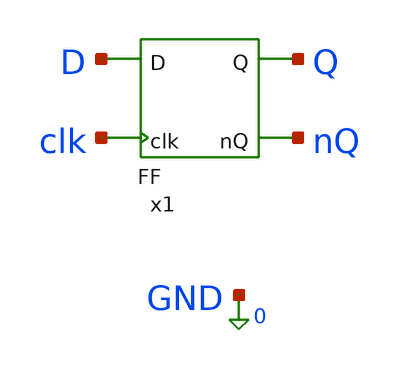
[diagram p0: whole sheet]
** sch_path: xschem_designs/FF_TB.sch
**.subckt FF_TB
x1 D Q nQ clk FF
**** begin user architecture code


.global VDD GND BP BN
.option temp=27
.include /usr/local/share/pdk/gf180mcuC/libs.tech/ngspice/design.ngspice
.lib /usr/local/share/pdk/gf180mcuC/libs.tech/ngspice/sm141064.ngspice typical

Vdd VDD 0 3.3
Vbp BP VDD 2.7
Vbn BN GND -2.7
VD D 0 PWL(0n 0 14.9n 0 15.1n 1.4 74.9n 1.4 75.1n 3.3 134.9n 3.3 135.1n 1.4 194.9n 1.4 195.1n 0
+ 254.9n 0 255.1n 3.3 314.9n 3.3 315.1n 0 374.9n 0 375.1n 0 434.9ns 0 435.1n 1.4 494.9n 1.4 495.1n 1.4
+ 554.9n 1.4 555.1n 3.3 615n 3.3)
Vclk clk 0 PULSE(3.3 0 29.9n 0.2n 0.2n 29.8n 60n)

.control
  save all
  tran 0.05n 615n
  write FF_TB.raw
.endc
.end


**** end user architecture code
**.ends

* expanding   symbol:  xschem_designs/FF.sym # of pins=4
** sym_path: xschem_designs/FF.sym
** sch_path: xschem_designs/FF.sch
.subckt FF D Q nQ clk
*.opin nQ
*.opin Q
*.ipin clk
*.ipin D
XM21 nclk clk VDD VDD pfet_03v3 L=0.28u W=0.44u nf=1 ad='int((nf+1)/2) * W/nf * 0.18u' as='int((nf+2)/2) * W/nf * 0.18u'
+ pd='2*int((nf+1)/2) * (W/nf + 0.18u)' ps='2*int((nf+2)/2) * (W/nf + 0.18u)' nrd='0.18u / W' nrs='0.18u / W'
+ sa=0 sb=0 sd=0 m=1 par=1
XM29 nclk clk GND GND nfet_03v3 L=0.28u W=0.22u nf=1 ad='int((nf+1)/2) * W/nf * 0.18u' as='int((nf+2)/2) * W/nf * 0.18u'
+ pd='2*int((nf+1)/2) * (W/nf + 0.18u)' ps='2*int((nf+2)/2) * (W/nf + 0.18u)' nrd='0.18u / W' nrs='0.18u / W'
+ sa=0 sb=0 sd=0 m=1 par=1
XM1 net1 nQ VDD VDD pfet_03v3 L=0.28u W=0.44u nf=1 ad='int((nf+1)/2) * W/nf * 0.18u' as='int((nf+2)/2) * W/nf * 0.18u'
+ pd='2*int((nf+1)/2) * (W/nf + 0.18u)' ps='2*int((nf+2)/2) * (W/nf + 0.18u)' nrd='0.18u / W' nrs='0.18u / W'
+ sa=0 sb=0 sd=0 m=1 par=1
XM22 Q Q net1 VDD pfet_03v3 L=2.24u W=0.44u nf=1 ad='int((nf+1)/2) * W/nf * 0.18u' as='int((nf+2)/2) * W/nf * 0.18u'
+ pd='2*int((nf+1)/2) * (W/nf + 0.18u)' ps='2*int((nf+2)/2) * (W/nf + 0.18u)' nrd='0.18u / W' nrs='0.18u / W'
+ sa=0 sb=0 sd=0 m=1 par=1
XM23 Q nQ VDD BP pfet_06v0 L=1.1u W=0.60u nf=1 ad='int((nf+1)/2) * W/nf * 0.18u' as='int((nf+2)/2) * W/nf * 0.18u'
+ pd='2*int((nf+1)/2) * (W/nf + 0.18u)' ps='2*int((nf+2)/2) * (W/nf + 0.18u)' nrd='0.18u / W' nrs='0.18u / W'
+ sa=0 sb=0 sd=0 m=1 par=1
XM24 Q S2 VDD BP pfet_06v0 L=1.1u W=0.60u nf=1 ad='int((nf+1)/2) * W/nf * 0.18u' as='int((nf+2)/2) * W/nf * 0.18u'
+ pd='2*int((nf+1)/2) * (W/nf + 0.18u)' ps='2*int((nf+2)/2) * (W/nf + 0.18u)' nrd='0.18u / W' nrs='0.18u / W'
+ sa=0 sb=0 sd=0 m=1 par=1
XM25 net1 S2 VDD VDD pfet_03v3 L=0.28u W=0.44u nf=1 ad='int((nf+1)/2) * W/nf * 0.18u' as='int((nf+2)/2) * W/nf * 0.18u'
+ pd='2*int((nf+1)/2) * (W/nf + 0.18u)' ps='2*int((nf+2)/2) * (W/nf + 0.18u)' nrd='0.18u / W' nrs='0.18u / W'
+ sa=0 sb=0 sd=0 m=1 par=1
XM26 Q Q net9 GND nfet_03v3 L=2.24u W=0.22u nf=1 ad='int((nf+1)/2) * W/nf * 0.18u' as='int((nf+2)/2) * W/nf * 0.18u'
+ pd='2*int((nf+1)/2) * (W/nf + 0.18u)' ps='2*int((nf+2)/2) * (W/nf + 0.18u)' nrd='0.18u / W' nrs='0.18u / W'
+ sa=0 sb=0 sd=0 m=1 par=1
XM27 net10 nQ GND BN nfet_06v0 L=1.4u W=0.30u nf=1 ad='int((nf+1)/2) * W/nf * 0.18u' as='int((nf+2)/2) * W/nf * 0.18u'
+ pd='2*int((nf+1)/2) * (W/nf + 0.18u)' ps='2*int((nf+2)/2) * (W/nf + 0.18u)' nrd='0.18u / W' nrs='0.18u / W'
+ sa=0 sb=0 sd=0 m=1 par=1
XM28 Q S2 net10 BN nfet_06v0 L=1.4u W=0.30u nf=1 ad='int((nf+1)/2) * W/nf * 0.18u' as='int((nf+2)/2) * W/nf * 0.18u'
+ pd='2*int((nf+1)/2) * (W/nf + 0.18u)' ps='2*int((nf+2)/2) * (W/nf + 0.18u)' nrd='0.18u / W' nrs='0.18u / W'
+ sa=0 sb=0 sd=0 m=1 par=1
XM2 net11 nQ GND GND nfet_03v3 L=0.28u W=0.22u nf=1 ad='int((nf+1)/2) * W/nf * 0.18u' as='int((nf+2)/2) * W/nf * 0.18u'
+ pd='2*int((nf+1)/2) * (W/nf + 0.18u)' ps='2*int((nf+2)/2) * (W/nf + 0.18u)' nrd='0.18u / W' nrs='0.18u / W'
+ sa=0 sb=0 sd=0 m=1 par=1
XM30 net9 S2 net11 GND nfet_03v3 L=0.28u W=0.22u nf=1 ad='int((nf+1)/2) * W/nf * 0.18u' as='int((nf+2)/2) * W/nf * 0.18u'
+ pd='2*int((nf+1)/2) * (W/nf + 0.18u)' ps='2*int((nf+2)/2) * (W/nf + 0.18u)' nrd='0.18u / W' nrs='0.18u / W'
+ sa=0 sb=0 sd=0 m=1 par=1
XM225 nD nD net12 GND nfet_03v3 L=2.24u W=0.22u nf=1 ad='int((nf+1)/2) * W/nf * 0.18u' as='int((nf+2)/2) * W/nf * 0.18u'
+ pd='2*int((nf+1)/2) * (W/nf + 0.18u)' ps='2*int((nf+2)/2) * (W/nf + 0.18u)' nrd='0.18u / W' nrs='0.18u / W'
+ sa=0 sb=0 sd=0 m=1 par=1
XM226 nD nD net13 VDD pfet_03v3 L=1.12u W=0.22u nf=1 ad='int((nf+1)/2) * W/nf * 0.18u' as='int((nf+2)/2) * W/nf * 0.18u'
+ pd='2*int((nf+1)/2) * (W/nf + 0.18u)' ps='2*int((nf+2)/2) * (W/nf + 0.18u)' nrd='0.18u / W' nrs='0.18u / W'
+ sa=0 sb=0 sd=0 m=1 par=1
XM237 net13 D VDD VDD pfet_03v3 L=0.28u W=0.44u nf=1 ad='int((nf+1)/2) * W/nf * 0.18u' as='int((nf+2)/2) * W/nf * 0.18u'
+ pd='2*int((nf+1)/2) * (W/nf + 0.18u)' ps='2*int((nf+2)/2) * (W/nf + 0.18u)' nrd='0.18u / W' nrs='0.18u / W'
+ sa=0 sb=0 sd=0 m=1 par=1
XM238 net12 D GND GND nfet_03v3 L=0.28u W=0.22u nf=1 ad='int((nf+1)/2) * W/nf * 0.18u' as='int((nf+2)/2) * W/nf * 0.18u'
+ pd='2*int((nf+1)/2) * (W/nf + 0.18u)' ps='2*int((nf+2)/2) * (W/nf + 0.18u)' nrd='0.18u / W' nrs='0.18u / W'
+ sa=0 sb=0 sd=0 m=1 par=1
XM241 nD D VDD BP pfet_06v0 L=1.1u W=0.60u nf=1 ad='int((nf+1)/2) * W/nf * 0.18u' as='int((nf+2)/2) * W/nf * 0.18u'
+ pd='2*int((nf+1)/2) * (W/nf + 0.18u)' ps='2*int((nf+2)/2) * (W/nf + 0.18u)' nrd='0.18u / W' nrs='0.18u / W'
+ sa=0 sb=0 sd=0 m=1 par=1
XM242 nD D GND BN nfet_06v0 L=1.4u W=0.30u nf=1 ad='int((nf+1)/2) * W/nf * 0.18u' as='int((nf+2)/2) * W/nf * 0.18u'
+ pd='2*int((nf+1)/2) * (W/nf + 0.18u)' ps='2*int((nf+2)/2) * (W/nf + 0.18u)' nrd='0.18u / W' nrs='0.18u / W'
+ sa=0 sb=0 sd=0 m=1 par=1
XM3 net2 Q VDD VDD pfet_03v3 L=0.28u W=0.44u nf=1 ad='int((nf+1)/2) * W/nf * 0.18u' as='int((nf+2)/2) * W/nf * 0.18u'
+ pd='2*int((nf+1)/2) * (W/nf + 0.18u)' ps='2*int((nf+2)/2) * (W/nf + 0.18u)' nrd='0.18u / W' nrs='0.18u / W'
+ sa=0 sb=0 sd=0 m=1 par=1
XM4 nQ nQ net2 VDD pfet_03v3 L=2.24u W=0.44u nf=1 ad='int((nf+1)/2) * W/nf * 0.18u' as='int((nf+2)/2) * W/nf * 0.18u'
+ pd='2*int((nf+1)/2) * (W/nf + 0.18u)' ps='2*int((nf+2)/2) * (W/nf + 0.18u)' nrd='0.18u / W' nrs='0.18u / W'
+ sa=0 sb=0 sd=0 m=1 par=1
XM5 nQ Q VDD BP pfet_06v0 L=1.1u W=0.60u nf=1 ad='int((nf+1)/2) * W/nf * 0.18u' as='int((nf+2)/2) * W/nf * 0.18u'
+ pd='2*int((nf+1)/2) * (W/nf + 0.18u)' ps='2*int((nf+2)/2) * (W/nf + 0.18u)' nrd='0.18u / W' nrs='0.18u / W'
+ sa=0 sb=0 sd=0 m=1 par=1
XM6 nQ R2 VDD BP pfet_06v0 L=1.1u W=0.60u nf=1 ad='int((nf+1)/2) * W/nf * 0.18u' as='int((nf+2)/2) * W/nf * 0.18u'
+ pd='2*int((nf+1)/2) * (W/nf + 0.18u)' ps='2*int((nf+2)/2) * (W/nf + 0.18u)' nrd='0.18u / W' nrs='0.18u / W'
+ sa=0 sb=0 sd=0 m=1 par=1
XM7 net2 R2 VDD VDD pfet_03v3 L=0.28u W=0.44u nf=1 ad='int((nf+1)/2) * W/nf * 0.18u' as='int((nf+2)/2) * W/nf * 0.18u'
+ pd='2*int((nf+1)/2) * (W/nf + 0.18u)' ps='2*int((nf+2)/2) * (W/nf + 0.18u)' nrd='0.18u / W' nrs='0.18u / W'
+ sa=0 sb=0 sd=0 m=1 par=1
XM8 nQ nQ net14 GND nfet_03v3 L=2.24u W=0.22u nf=1 ad='int((nf+1)/2) * W/nf * 0.18u' as='int((nf+2)/2) * W/nf * 0.18u'
+ pd='2*int((nf+1)/2) * (W/nf + 0.18u)' ps='2*int((nf+2)/2) * (W/nf + 0.18u)' nrd='0.18u / W' nrs='0.18u / W'
+ sa=0 sb=0 sd=0 m=1 par=1
XM9 net15 Q GND BN nfet_06v0 L=1.4u W=0.30u nf=1 ad='int((nf+1)/2) * W/nf * 0.18u' as='int((nf+2)/2) * W/nf * 0.18u'
+ pd='2*int((nf+1)/2) * (W/nf + 0.18u)' ps='2*int((nf+2)/2) * (W/nf + 0.18u)' nrd='0.18u / W' nrs='0.18u / W'
+ sa=0 sb=0 sd=0 m=1 par=1
XM10 nQ R2 net15 BN nfet_06v0 L=1.4u W=0.30u nf=1 ad='int((nf+1)/2) * W/nf * 0.18u' as='int((nf+2)/2) * W/nf * 0.18u'
+ pd='2*int((nf+1)/2) * (W/nf + 0.18u)' ps='2*int((nf+2)/2) * (W/nf + 0.18u)' nrd='0.18u / W' nrs='0.18u / W'
+ sa=0 sb=0 sd=0 m=1 par=1
XM11 net16 Q GND GND nfet_03v3 L=0.28u W=0.22u nf=1 ad='int((nf+1)/2) * W/nf * 0.18u' as='int((nf+2)/2) * W/nf * 0.18u'
+ pd='2*int((nf+1)/2) * (W/nf + 0.18u)' ps='2*int((nf+2)/2) * (W/nf + 0.18u)' nrd='0.18u / W' nrs='0.18u / W'
+ sa=0 sb=0 sd=0 m=1 par=1
XM12 net14 R2 net16 GND nfet_03v3 L=0.28u W=0.22u nf=1 ad='int((nf+1)/2) * W/nf * 0.18u' as='int((nf+2)/2) * W/nf * 0.18u'
+ pd='2*int((nf+1)/2) * (W/nf + 0.18u)' ps='2*int((nf+2)/2) * (W/nf + 0.18u)' nrd='0.18u / W' nrs='0.18u / W'
+ sa=0 sb=0 sd=0 m=1 par=1
XM13 net3 Qi VDD VDD pfet_03v3 L=0.28u W=0.44u nf=1 ad='int((nf+1)/2) * W/nf * 0.18u' as='int((nf+2)/2) * W/nf * 0.18u'
+ pd='2*int((nf+1)/2) * (W/nf + 0.18u)' ps='2*int((nf+2)/2) * (W/nf + 0.18u)' nrd='0.18u / W' nrs='0.18u / W'
+ sa=0 sb=0 sd=0 m=1 par=1
XM14 S2 S2 net3 VDD pfet_03v3 L=2.24u W=0.44u nf=1 ad='int((nf+1)/2) * W/nf * 0.18u' as='int((nf+2)/2) * W/nf * 0.18u'
+ pd='2*int((nf+1)/2) * (W/nf + 0.18u)' ps='2*int((nf+2)/2) * (W/nf + 0.18u)' nrd='0.18u / W' nrs='0.18u / W'
+ sa=0 sb=0 sd=0 m=1 par=1
XM15 S2 Qi VDD BP pfet_06v0 L=1.1u W=0.60u nf=1 ad='int((nf+1)/2) * W/nf * 0.18u' as='int((nf+2)/2) * W/nf * 0.18u'
+ pd='2*int((nf+1)/2) * (W/nf + 0.18u)' ps='2*int((nf+2)/2) * (W/nf + 0.18u)' nrd='0.18u / W' nrs='0.18u / W'
+ sa=0 sb=0 sd=0 m=1 par=1
XM16 S2 nclk VDD BP pfet_06v0 L=1.1u W=0.60u nf=1 ad='int((nf+1)/2) * W/nf * 0.18u' as='int((nf+2)/2) * W/nf * 0.18u'
+ pd='2*int((nf+1)/2) * (W/nf + 0.18u)' ps='2*int((nf+2)/2) * (W/nf + 0.18u)' nrd='0.18u / W' nrs='0.18u / W'
+ sa=0 sb=0 sd=0 m=1 par=1
XM17 net3 nclk VDD VDD pfet_03v3 L=0.28u W=0.44u nf=1 ad='int((nf+1)/2) * W/nf * 0.18u' as='int((nf+2)/2) * W/nf * 0.18u'
+ pd='2*int((nf+1)/2) * (W/nf + 0.18u)' ps='2*int((nf+2)/2) * (W/nf + 0.18u)' nrd='0.18u / W' nrs='0.18u / W'
+ sa=0 sb=0 sd=0 m=1 par=1
XM18 S2 S2 net17 GND nfet_03v3 L=2.24u W=0.22u nf=1 ad='int((nf+1)/2) * W/nf * 0.18u' as='int((nf+2)/2) * W/nf * 0.18u'
+ pd='2*int((nf+1)/2) * (W/nf + 0.18u)' ps='2*int((nf+2)/2) * (W/nf + 0.18u)' nrd='0.18u / W' nrs='0.18u / W'
+ sa=0 sb=0 sd=0 m=1 par=1
XM19 net18 Qi GND BN nfet_06v0 L=1.4u W=0.30u nf=1 ad='int((nf+1)/2) * W/nf * 0.18u' as='int((nf+2)/2) * W/nf * 0.18u'
+ pd='2*int((nf+1)/2) * (W/nf + 0.18u)' ps='2*int((nf+2)/2) * (W/nf + 0.18u)' nrd='0.18u / W' nrs='0.18u / W'
+ sa=0 sb=0 sd=0 m=1 par=1
XM20 S2 nclk net18 BN nfet_06v0 L=1.4u W=0.30u nf=1 ad='int((nf+1)/2) * W/nf * 0.18u' as='int((nf+2)/2) * W/nf * 0.18u'
+ pd='2*int((nf+1)/2) * (W/nf + 0.18u)' ps='2*int((nf+2)/2) * (W/nf + 0.18u)' nrd='0.18u / W' nrs='0.18u / W'
+ sa=0 sb=0 sd=0 m=1 par=1
XM31 net19 Qi GND GND nfet_03v3 L=0.28u W=0.22u nf=1 ad='int((nf+1)/2) * W/nf * 0.18u' as='int((nf+2)/2) * W/nf * 0.18u'
+ pd='2*int((nf+1)/2) * (W/nf + 0.18u)' ps='2*int((nf+2)/2) * (W/nf + 0.18u)' nrd='0.18u / W' nrs='0.18u / W'
+ sa=0 sb=0 sd=0 m=1 par=1
XM32 net17 nclk net19 GND nfet_03v3 L=0.28u W=0.22u nf=1 ad='int((nf+1)/2) * W/nf * 0.18u' as='int((nf+2)/2) * W/nf * 0.18u'
+ pd='2*int((nf+1)/2) * (W/nf + 0.18u)' ps='2*int((nf+2)/2) * (W/nf + 0.18u)' nrd='0.18u / W' nrs='0.18u / W'
+ sa=0 sb=0 sd=0 m=1 par=1
XM33 net4 nQi VDD VDD pfet_03v3 L=0.28u W=0.44u nf=1 ad='int((nf+1)/2) * W/nf * 0.18u' as='int((nf+2)/2) * W/nf * 0.18u'
+ pd='2*int((nf+1)/2) * (W/nf + 0.18u)' ps='2*int((nf+2)/2) * (W/nf + 0.18u)' nrd='0.18u / W' nrs='0.18u / W'
+ sa=0 sb=0 sd=0 m=1 par=1
XM34 R2 R2 net4 VDD pfet_03v3 L=2.24u W=0.44u nf=1 ad='int((nf+1)/2) * W/nf * 0.18u' as='int((nf+2)/2) * W/nf * 0.18u'
+ pd='2*int((nf+1)/2) * (W/nf + 0.18u)' ps='2*int((nf+2)/2) * (W/nf + 0.18u)' nrd='0.18u / W' nrs='0.18u / W'
+ sa=0 sb=0 sd=0 m=1 par=1
XM35 R2 nQi VDD BP pfet_06v0 L=1.1u W=0.60u nf=1 ad='int((nf+1)/2) * W/nf * 0.18u' as='int((nf+2)/2) * W/nf * 0.18u'
+ pd='2*int((nf+1)/2) * (W/nf + 0.18u)' ps='2*int((nf+2)/2) * (W/nf + 0.18u)' nrd='0.18u / W' nrs='0.18u / W'
+ sa=0 sb=0 sd=0 m=1 par=1
XM36 R2 nclk VDD BP pfet_06v0 L=1.1u W=0.60u nf=1 ad='int((nf+1)/2) * W/nf * 0.18u' as='int((nf+2)/2) * W/nf * 0.18u'
+ pd='2*int((nf+1)/2) * (W/nf + 0.18u)' ps='2*int((nf+2)/2) * (W/nf + 0.18u)' nrd='0.18u / W' nrs='0.18u / W'
+ sa=0 sb=0 sd=0 m=1 par=1
XM37 net4 nclk VDD VDD pfet_03v3 L=0.28u W=0.44u nf=1 ad='int((nf+1)/2) * W/nf * 0.18u' as='int((nf+2)/2) * W/nf * 0.18u'
+ pd='2*int((nf+1)/2) * (W/nf + 0.18u)' ps='2*int((nf+2)/2) * (W/nf + 0.18u)' nrd='0.18u / W' nrs='0.18u / W'
+ sa=0 sb=0 sd=0 m=1 par=1
XM38 R2 R2 net20 GND nfet_03v3 L=2.24u W=0.22u nf=1 ad='int((nf+1)/2) * W/nf * 0.18u' as='int((nf+2)/2) * W/nf * 0.18u'
+ pd='2*int((nf+1)/2) * (W/nf + 0.18u)' ps='2*int((nf+2)/2) * (W/nf + 0.18u)' nrd='0.18u / W' nrs='0.18u / W'
+ sa=0 sb=0 sd=0 m=1 par=1
XM39 net21 nQi GND BN nfet_06v0 L=1.4u W=0.30u nf=1 ad='int((nf+1)/2) * W/nf * 0.18u' as='int((nf+2)/2) * W/nf * 0.18u'
+ pd='2*int((nf+1)/2) * (W/nf + 0.18u)' ps='2*int((nf+2)/2) * (W/nf + 0.18u)' nrd='0.18u / W' nrs='0.18u / W'
+ sa=0 sb=0 sd=0 m=1 par=1
XM40 R2 nclk net21 BN nfet_06v0 L=1.4u W=0.30u nf=1 ad='int((nf+1)/2) * W/nf * 0.18u' as='int((nf+2)/2) * W/nf * 0.18u'
+ pd='2*int((nf+1)/2) * (W/nf + 0.18u)' ps='2*int((nf+2)/2) * (W/nf + 0.18u)' nrd='0.18u / W' nrs='0.18u / W'
+ sa=0 sb=0 sd=0 m=1 par=1
XM41 net22 nQi GND GND nfet_03v3 L=0.28u W=0.22u nf=1 ad='int((nf+1)/2) * W/nf * 0.18u' as='int((nf+2)/2) * W/nf * 0.18u'
+ pd='2*int((nf+1)/2) * (W/nf + 0.18u)' ps='2*int((nf+2)/2) * (W/nf + 0.18u)' nrd='0.18u / W' nrs='0.18u / W'
+ sa=0 sb=0 sd=0 m=1 par=1
XM42 net20 nclk net22 GND nfet_03v3 L=0.28u W=0.22u nf=1 ad='int((nf+1)/2) * W/nf * 0.18u' as='int((nf+2)/2) * W/nf * 0.18u'
+ pd='2*int((nf+1)/2) * (W/nf + 0.18u)' ps='2*int((nf+2)/2) * (W/nf + 0.18u)' nrd='0.18u / W' nrs='0.18u / W'
+ sa=0 sb=0 sd=0 m=1 par=1
XM53 net5 nQi VDD VDD pfet_03v3 L=0.28u W=0.44u nf=1 ad='int((nf+1)/2) * W/nf * 0.18u' as='int((nf+2)/2) * W/nf * 0.18u'
+ pd='2*int((nf+1)/2) * (W/nf + 0.18u)' ps='2*int((nf+2)/2) * (W/nf + 0.18u)' nrd='0.18u / W' nrs='0.18u / W'
+ sa=0 sb=0 sd=0 m=1 par=1
XM54 Qi Qi net5 VDD pfet_03v3 L=2.24u W=0.44u nf=1 ad='int((nf+1)/2) * W/nf * 0.18u' as='int((nf+2)/2) * W/nf * 0.18u'
+ pd='2*int((nf+1)/2) * (W/nf + 0.18u)' ps='2*int((nf+2)/2) * (W/nf + 0.18u)' nrd='0.18u / W' nrs='0.18u / W'
+ sa=0 sb=0 sd=0 m=1 par=1
XM55 Qi nQi VDD BP pfet_06v0 L=1.1u W=0.60u nf=1 ad='int((nf+1)/2) * W/nf * 0.18u' as='int((nf+2)/2) * W/nf * 0.18u'
+ pd='2*int((nf+1)/2) * (W/nf + 0.18u)' ps='2*int((nf+2)/2) * (W/nf + 0.18u)' nrd='0.18u / W' nrs='0.18u / W'
+ sa=0 sb=0 sd=0 m=1 par=1
XM56 Qi S1 VDD BP pfet_06v0 L=1.1u W=0.60u nf=1 ad='int((nf+1)/2) * W/nf * 0.18u' as='int((nf+2)/2) * W/nf * 0.18u'
+ pd='2*int((nf+1)/2) * (W/nf + 0.18u)' ps='2*int((nf+2)/2) * (W/nf + 0.18u)' nrd='0.18u / W' nrs='0.18u / W'
+ sa=0 sb=0 sd=0 m=1 par=1
XM57 net5 S1 VDD VDD pfet_03v3 L=0.28u W=0.44u nf=1 ad='int((nf+1)/2) * W/nf * 0.18u' as='int((nf+2)/2) * W/nf * 0.18u'
+ pd='2*int((nf+1)/2) * (W/nf + 0.18u)' ps='2*int((nf+2)/2) * (W/nf + 0.18u)' nrd='0.18u / W' nrs='0.18u / W'
+ sa=0 sb=0 sd=0 m=1 par=1
XM58 Qi Qi net23 GND nfet_03v3 L=2.24u W=0.22u nf=1 ad='int((nf+1)/2) * W/nf * 0.18u' as='int((nf+2)/2) * W/nf * 0.18u'
+ pd='2*int((nf+1)/2) * (W/nf + 0.18u)' ps='2*int((nf+2)/2) * (W/nf + 0.18u)' nrd='0.18u / W' nrs='0.18u / W'
+ sa=0 sb=0 sd=0 m=1 par=1
XM59 net24 nQi GND BN nfet_06v0 L=1.4u W=0.30u nf=1 ad='int((nf+1)/2) * W/nf * 0.18u' as='int((nf+2)/2) * W/nf * 0.18u'
+ pd='2*int((nf+1)/2) * (W/nf + 0.18u)' ps='2*int((nf+2)/2) * (W/nf + 0.18u)' nrd='0.18u / W' nrs='0.18u / W'
+ sa=0 sb=0 sd=0 m=1 par=1
XM60 Qi S1 net24 BN nfet_06v0 L=1.4u W=0.30u nf=1 ad='int((nf+1)/2) * W/nf * 0.18u' as='int((nf+2)/2) * W/nf * 0.18u'
+ pd='2*int((nf+1)/2) * (W/nf + 0.18u)' ps='2*int((nf+2)/2) * (W/nf + 0.18u)' nrd='0.18u / W' nrs='0.18u / W'
+ sa=0 sb=0 sd=0 m=1 par=1
XM61 net25 nQi GND GND nfet_03v3 L=0.28u W=0.22u nf=1 ad='int((nf+1)/2) * W/nf * 0.18u' as='int((nf+2)/2) * W/nf * 0.18u'
+ pd='2*int((nf+1)/2) * (W/nf + 0.18u)' ps='2*int((nf+2)/2) * (W/nf + 0.18u)' nrd='0.18u / W' nrs='0.18u / W'
+ sa=0 sb=0 sd=0 m=1 par=1
XM62 net23 S1 net25 GND nfet_03v3 L=0.28u W=0.22u nf=1 ad='int((nf+1)/2) * W/nf * 0.18u' as='int((nf+2)/2) * W/nf * 0.18u'
+ pd='2*int((nf+1)/2) * (W/nf + 0.18u)' ps='2*int((nf+2)/2) * (W/nf + 0.18u)' nrd='0.18u / W' nrs='0.18u / W'
+ sa=0 sb=0 sd=0 m=1 par=1
XM63 net6 Qi VDD VDD pfet_03v3 L=0.28u W=0.44u nf=1 ad='int((nf+1)/2) * W/nf * 0.18u' as='int((nf+2)/2) * W/nf * 0.18u'
+ pd='2*int((nf+1)/2) * (W/nf + 0.18u)' ps='2*int((nf+2)/2) * (W/nf + 0.18u)' nrd='0.18u / W' nrs='0.18u / W'
+ sa=0 sb=0 sd=0 m=1 par=1
XM64 nQi nQi net6 VDD pfet_03v3 L=2.24u W=0.44u nf=1 ad='int((nf+1)/2) * W/nf * 0.18u' as='int((nf+2)/2) * W/nf * 0.18u'
+ pd='2*int((nf+1)/2) * (W/nf + 0.18u)' ps='2*int((nf+2)/2) * (W/nf + 0.18u)' nrd='0.18u / W' nrs='0.18u / W'
+ sa=0 sb=0 sd=0 m=1 par=1
XM65 nQi Qi VDD BP pfet_06v0 L=1.1u W=0.60u nf=1 ad='int((nf+1)/2) * W/nf * 0.18u' as='int((nf+2)/2) * W/nf * 0.18u'
+ pd='2*int((nf+1)/2) * (W/nf + 0.18u)' ps='2*int((nf+2)/2) * (W/nf + 0.18u)' nrd='0.18u / W' nrs='0.18u / W'
+ sa=0 sb=0 sd=0 m=1 par=1
XM66 nQi R1 VDD BP pfet_06v0 L=1.1u W=0.60u nf=1 ad='int((nf+1)/2) * W/nf * 0.18u' as='int((nf+2)/2) * W/nf * 0.18u'
+ pd='2*int((nf+1)/2) * (W/nf + 0.18u)' ps='2*int((nf+2)/2) * (W/nf + 0.18u)' nrd='0.18u / W' nrs='0.18u / W'
+ sa=0 sb=0 sd=0 m=1 par=1
XM67 net6 R1 VDD VDD pfet_03v3 L=0.28u W=0.44u nf=1 ad='int((nf+1)/2) * W/nf * 0.18u' as='int((nf+2)/2) * W/nf * 0.18u'
+ pd='2*int((nf+1)/2) * (W/nf + 0.18u)' ps='2*int((nf+2)/2) * (W/nf + 0.18u)' nrd='0.18u / W' nrs='0.18u / W'
+ sa=0 sb=0 sd=0 m=1 par=1
XM68 nQi nQi net26 GND nfet_03v3 L=2.24u W=0.22u nf=1 ad='int((nf+1)/2) * W/nf * 0.18u' as='int((nf+2)/2) * W/nf * 0.18u'
+ pd='2*int((nf+1)/2) * (W/nf + 0.18u)' ps='2*int((nf+2)/2) * (W/nf + 0.18u)' nrd='0.18u / W' nrs='0.18u / W'
+ sa=0 sb=0 sd=0 m=1 par=1
XM69 net27 Qi GND BN nfet_06v0 L=1.4u W=0.30u nf=1 ad='int((nf+1)/2) * W/nf * 0.18u' as='int((nf+2)/2) * W/nf * 0.18u'
+ pd='2*int((nf+1)/2) * (W/nf + 0.18u)' ps='2*int((nf+2)/2) * (W/nf + 0.18u)' nrd='0.18u / W' nrs='0.18u / W'
+ sa=0 sb=0 sd=0 m=1 par=1
XM70 nQi R1 net27 BN nfet_06v0 L=1.4u W=0.30u nf=1 ad='int((nf+1)/2) * W/nf * 0.18u' as='int((nf+2)/2) * W/nf * 0.18u'
+ pd='2*int((nf+1)/2) * (W/nf + 0.18u)' ps='2*int((nf+2)/2) * (W/nf + 0.18u)' nrd='0.18u / W' nrs='0.18u / W'
+ sa=0 sb=0 sd=0 m=1 par=1
XM71 net28 Qi GND GND nfet_03v3 L=0.28u W=0.22u nf=1 ad='int((nf+1)/2) * W/nf * 0.18u' as='int((nf+2)/2) * W/nf * 0.18u'
+ pd='2*int((nf+1)/2) * (W/nf + 0.18u)' ps='2*int((nf+2)/2) * (W/nf + 0.18u)' nrd='0.18u / W' nrs='0.18u / W'
+ sa=0 sb=0 sd=0 m=1 par=1
XM72 net26 R1 net28 GND nfet_03v3 L=0.28u W=0.22u nf=1 ad='int((nf+1)/2) * W/nf * 0.18u' as='int((nf+2)/2) * W/nf * 0.18u'
+ pd='2*int((nf+1)/2) * (W/nf + 0.18u)' ps='2*int((nf+2)/2) * (W/nf + 0.18u)' nrd='0.18u / W' nrs='0.18u / W'
+ sa=0 sb=0 sd=0 m=1 par=1
XM73 net7 D VDD VDD pfet_03v3 L=0.28u W=0.44u nf=1 ad='int((nf+1)/2) * W/nf * 0.18u' as='int((nf+2)/2) * W/nf * 0.18u'
+ pd='2*int((nf+1)/2) * (W/nf + 0.18u)' ps='2*int((nf+2)/2) * (W/nf + 0.18u)' nrd='0.18u / W' nrs='0.18u / W'
+ sa=0 sb=0 sd=0 m=1 par=1
XM74 S1 S1 net7 VDD pfet_03v3 L=2.24u W=0.44u nf=1 ad='int((nf+1)/2) * W/nf * 0.18u' as='int((nf+2)/2) * W/nf * 0.18u'
+ pd='2*int((nf+1)/2) * (W/nf + 0.18u)' ps='2*int((nf+2)/2) * (W/nf + 0.18u)' nrd='0.18u / W' nrs='0.18u / W'
+ sa=0 sb=0 sd=0 m=1 par=1
XM75 S1 D VDD BP pfet_06v0 L=1.1u W=0.60u nf=1 ad='int((nf+1)/2) * W/nf * 0.18u' as='int((nf+2)/2) * W/nf * 0.18u'
+ pd='2*int((nf+1)/2) * (W/nf + 0.18u)' ps='2*int((nf+2)/2) * (W/nf + 0.18u)' nrd='0.18u / W' nrs='0.18u / W'
+ sa=0 sb=0 sd=0 m=1 par=1
XM76 S1 clk VDD BP pfet_06v0 L=1.1u W=0.60u nf=1 ad='int((nf+1)/2) * W/nf * 0.18u' as='int((nf+2)/2) * W/nf * 0.18u'
+ pd='2*int((nf+1)/2) * (W/nf + 0.18u)' ps='2*int((nf+2)/2) * (W/nf + 0.18u)' nrd='0.18u / W' nrs='0.18u / W'
+ sa=0 sb=0 sd=0 m=1 par=1
XM77 net7 clk VDD VDD pfet_03v3 L=0.28u W=0.44u nf=1 ad='int((nf+1)/2) * W/nf * 0.18u' as='int((nf+2)/2) * W/nf * 0.18u'
+ pd='2*int((nf+1)/2) * (W/nf + 0.18u)' ps='2*int((nf+2)/2) * (W/nf + 0.18u)' nrd='0.18u / W' nrs='0.18u / W'
+ sa=0 sb=0 sd=0 m=1 par=1
XM78 S1 S1 net29 GND nfet_03v3 L=2.24u W=0.22u nf=1 ad='int((nf+1)/2) * W/nf * 0.18u' as='int((nf+2)/2) * W/nf * 0.18u'
+ pd='2*int((nf+1)/2) * (W/nf + 0.18u)' ps='2*int((nf+2)/2) * (W/nf + 0.18u)' nrd='0.18u / W' nrs='0.18u / W'
+ sa=0 sb=0 sd=0 m=1 par=1
XM79 net30 D GND BN nfet_06v0 L=1.4u W=0.30u nf=1 ad='int((nf+1)/2) * W/nf * 0.18u' as='int((nf+2)/2) * W/nf * 0.18u'
+ pd='2*int((nf+1)/2) * (W/nf + 0.18u)' ps='2*int((nf+2)/2) * (W/nf + 0.18u)' nrd='0.18u / W' nrs='0.18u / W'
+ sa=0 sb=0 sd=0 m=1 par=1
XM80 S1 clk net30 BN nfet_06v0 L=1.4u W=0.30u nf=1 ad='int((nf+1)/2) * W/nf * 0.18u' as='int((nf+2)/2) * W/nf * 0.18u'
+ pd='2*int((nf+1)/2) * (W/nf + 0.18u)' ps='2*int((nf+2)/2) * (W/nf + 0.18u)' nrd='0.18u / W' nrs='0.18u / W'
+ sa=0 sb=0 sd=0 m=1 par=1
XM81 net31 D GND GND nfet_03v3 L=0.28u W=0.22u nf=1 ad='int((nf+1)/2) * W/nf * 0.18u' as='int((nf+2)/2) * W/nf * 0.18u'
+ pd='2*int((nf+1)/2) * (W/nf + 0.18u)' ps='2*int((nf+2)/2) * (W/nf + 0.18u)' nrd='0.18u / W' nrs='0.18u / W'
+ sa=0 sb=0 sd=0 m=1 par=1
XM82 net29 clk net31 GND nfet_03v3 L=0.28u W=0.22u nf=1 ad='int((nf+1)/2) * W/nf * 0.18u' as='int((nf+2)/2) * W/nf * 0.18u'
+ pd='2*int((nf+1)/2) * (W/nf + 0.18u)' ps='2*int((nf+2)/2) * (W/nf + 0.18u)' nrd='0.18u / W' nrs='0.18u / W'
+ sa=0 sb=0 sd=0 m=1 par=1
XM83 net8 nD VDD VDD pfet_03v3 L=0.28u W=0.44u nf=1 ad='int((nf+1)/2) * W/nf * 0.18u' as='int((nf+2)/2) * W/nf * 0.18u'
+ pd='2*int((nf+1)/2) * (W/nf + 0.18u)' ps='2*int((nf+2)/2) * (W/nf + 0.18u)' nrd='0.18u / W' nrs='0.18u / W'
+ sa=0 sb=0 sd=0 m=1 par=1
XM84 R1 R1 net8 VDD pfet_03v3 L=2.24u W=0.44u nf=1 ad='int((nf+1)/2) * W/nf * 0.18u' as='int((nf+2)/2) * W/nf * 0.18u'
+ pd='2*int((nf+1)/2) * (W/nf + 0.18u)' ps='2*int((nf+2)/2) * (W/nf + 0.18u)' nrd='0.18u / W' nrs='0.18u / W'
+ sa=0 sb=0 sd=0 m=1 par=1
XM85 R1 nD VDD BP pfet_06v0 L=1.1u W=0.60u nf=1 ad='int((nf+1)/2) * W/nf * 0.18u' as='int((nf+2)/2) * W/nf * 0.18u'
+ pd='2*int((nf+1)/2) * (W/nf + 0.18u)' ps='2*int((nf+2)/2) * (W/nf + 0.18u)' nrd='0.18u / W' nrs='0.18u / W'
+ sa=0 sb=0 sd=0 m=1 par=1
XM86 R1 clk VDD BP pfet_06v0 L=1.1u W=0.60u nf=1 ad='int((nf+1)/2) * W/nf * 0.18u' as='int((nf+2)/2) * W/nf * 0.18u'
+ pd='2*int((nf+1)/2) * (W/nf + 0.18u)' ps='2*int((nf+2)/2) * (W/nf + 0.18u)' nrd='0.18u / W' nrs='0.18u / W'
+ sa=0 sb=0 sd=0 m=1 par=1
XM87 net8 clk VDD VDD pfet_03v3 L=0.28u W=0.44u nf=1 ad='int((nf+1)/2) * W/nf * 0.18u' as='int((nf+2)/2) * W/nf * 0.18u'
+ pd='2*int((nf+1)/2) * (W/nf + 0.18u)' ps='2*int((nf+2)/2) * (W/nf + 0.18u)' nrd='0.18u / W' nrs='0.18u / W'
+ sa=0 sb=0 sd=0 m=1 par=1
XM88 R1 R1 net32 GND nfet_03v3 L=2.24u W=0.22u nf=1 ad='int((nf+1)/2) * W/nf * 0.18u' as='int((nf+2)/2) * W/nf * 0.18u'
+ pd='2*int((nf+1)/2) * (W/nf + 0.18u)' ps='2*int((nf+2)/2) * (W/nf + 0.18u)' nrd='0.18u / W' nrs='0.18u / W'
+ sa=0 sb=0 sd=0 m=1 par=1
XM89 net33 nD GND BN nfet_06v0 L=1.4u W=0.30u nf=1 ad='int((nf+1)/2) * W/nf * 0.18u' as='int((nf+2)/2) * W/nf * 0.18u'
+ pd='2*int((nf+1)/2) * (W/nf + 0.18u)' ps='2*int((nf+2)/2) * (W/nf + 0.18u)' nrd='0.18u / W' nrs='0.18u / W'
+ sa=0 sb=0 sd=0 m=1 par=1
XM90 R1 clk net33 BN nfet_06v0 L=1.4u W=0.30u nf=1 ad='int((nf+1)/2) * W/nf * 0.18u' as='int((nf+2)/2) * W/nf * 0.18u'
+ pd='2*int((nf+1)/2) * (W/nf + 0.18u)' ps='2*int((nf+2)/2) * (W/nf + 0.18u)' nrd='0.18u / W' nrs='0.18u / W'
+ sa=0 sb=0 sd=0 m=1 par=1
XM91 net34 nD GND GND nfet_03v3 L=0.28u W=0.22u nf=1 ad='int((nf+1)/2) * W/nf * 0.18u' as='int((nf+2)/2) * W/nf * 0.18u'
+ pd='2*int((nf+1)/2) * (W/nf + 0.18u)' ps='2*int((nf+2)/2) * (W/nf + 0.18u)' nrd='0.18u / W' nrs='0.18u / W'
+ sa=0 sb=0 sd=0 m=1 par=1
XM92 net32 clk net34 GND nfet_03v3 L=0.28u W=0.22u nf=1 ad='int((nf+1)/2) * W/nf * 0.18u' as='int((nf+2)/2) * W/nf * 0.18u'
+ pd='2*int((nf+1)/2) * (W/nf + 0.18u)' ps='2*int((nf+2)/2) * (W/nf + 0.18u)' nrd='0.18u / W' nrs='0.18u / W'
+ sa=0 sb=0 sd=0 m=1 par=1
.ends

.end
